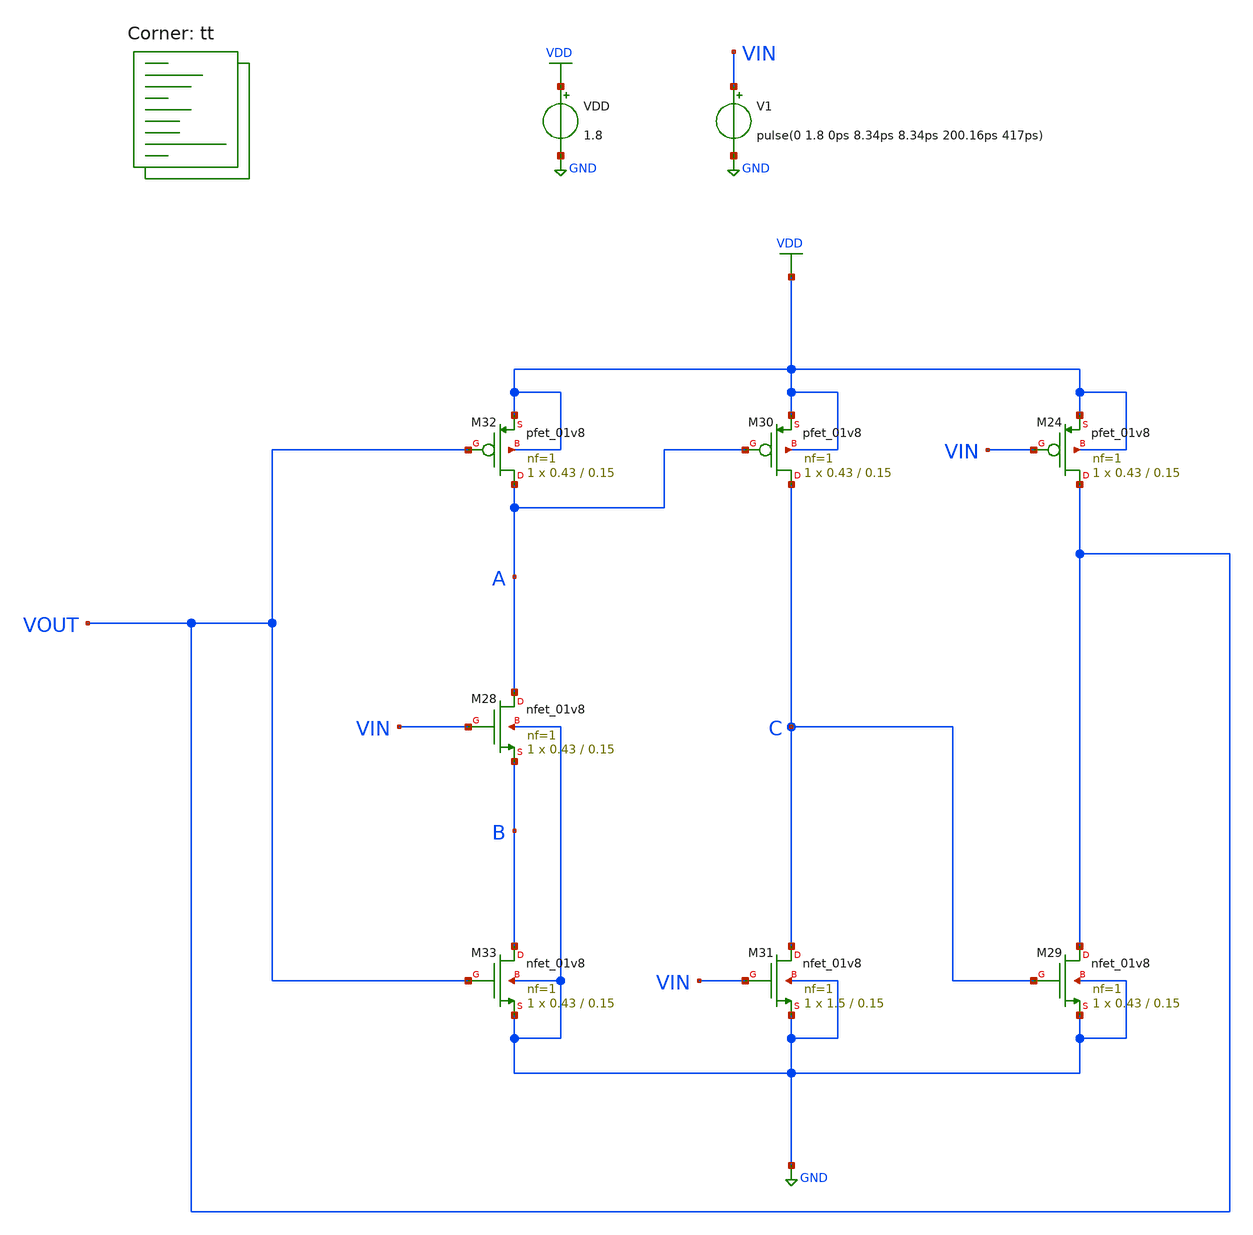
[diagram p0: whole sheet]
** sch_path: projects/pll/divider/xschem_ngspice/tb_TSPC_FF_ratioed_divide2_2.sch
**.subckt tb_TSPC_FF_ratioed_divide2_2
VDD VDD GND 1.8
V1 VIN GND pulse(0 1.8 0ps 8.34ps 8.34ps 200.16ps 417ps)
XM24 VOUT VIN VDD VDD sky130_fd_pr__pfet_01v8 L=0.15 W=0.43 nf=1 ad='int((nf+1)/2) * W/nf * 0.29' as='int((nf+2)/2) * W/nf * 0.29'
+ pd='2*int((nf+1)/2) * (W/nf + 0.29)' ps='2*int((nf+2)/2) * (W/nf + 0.29)' nrd='0.29 / W' nrs='0.29 / W'
+ sa=0 sb=0 sd=0 mult=1 m=1
XM29 VOUT C GND GND sky130_fd_pr__nfet_01v8 L=0.15 W=0.43 nf=1 ad='int((nf+1)/2) * W/nf * 0.29' as='int((nf+2)/2) * W/nf * 0.29'
+ pd='2*int((nf+1)/2) * (W/nf + 0.29)' ps='2*int((nf+2)/2) * (W/nf + 0.29)' nrd='0.29 / W' nrs='0.29 / W'
+ sa=0 sb=0 sd=0 mult=1 m=1
XM30 C A VDD VDD sky130_fd_pr__pfet_01v8 L=0.15 W=0.43 nf=1 ad='int((nf+1)/2) * W/nf * 0.29' as='int((nf+2)/2) * W/nf * 0.29'
+ pd='2*int((nf+1)/2) * (W/nf + 0.29)' ps='2*int((nf+2)/2) * (W/nf + 0.29)' nrd='0.29 / W' nrs='0.29 / W'
+ sa=0 sb=0 sd=0 mult=1 m=1
XM31 C VIN GND GND sky130_fd_pr__nfet_01v8 L=0.15 W=1.5 nf=1 ad='int((nf+1)/2) * W/nf * 0.29' as='int((nf+2)/2) * W/nf * 0.29'
+ pd='2*int((nf+1)/2) * (W/nf + 0.29)' ps='2*int((nf+2)/2) * (W/nf + 0.29)' nrd='0.29 / W' nrs='0.29 / W'
+ sa=0 sb=0 sd=0 mult=1 m=1
XM32 A VOUT VDD VDD sky130_fd_pr__pfet_01v8 L=0.15 W=0.43 nf=1 ad='int((nf+1)/2) * W/nf * 0.29' as='int((nf+2)/2) * W/nf * 0.29'
+ pd='2*int((nf+1)/2) * (W/nf + 0.29)' ps='2*int((nf+2)/2) * (W/nf + 0.29)' nrd='0.29 / W' nrs='0.29 / W'
+ sa=0 sb=0 sd=0 mult=1 m=1
XM33 B VOUT GND GND sky130_fd_pr__nfet_01v8 L=0.15 W=0.43 nf=1 ad='int((nf+1)/2) * W/nf * 0.29' as='int((nf+2)/2) * W/nf * 0.29'
+ pd='2*int((nf+1)/2) * (W/nf + 0.29)' ps='2*int((nf+2)/2) * (W/nf + 0.29)' nrd='0.29 / W' nrs='0.29 / W'
+ sa=0 sb=0 sd=0 mult=1 m=1
XM28 A VIN B GND sky130_fd_pr__nfet_01v8 L=0.15 W=0.43 nf=1 ad='int((nf+1)/2) * W/nf * 0.29' as='int((nf+2)/2) * W/nf * 0.29'
+ pd='2*int((nf+1)/2) * (W/nf + 0.29)' ps='2*int((nf+2)/2) * (W/nf + 0.29)' nrd='0.29 / W' nrs='0.29 / W'
+ sa=0 sb=0 sd=0 mult=1 m=1
**** begin user architecture code



.include /foss/pdks/sky130A/libs.ref/sky130_fd_sc_hd/spice/sky130_fd_sc_hd.spice

.option method=gear
.option wnflag=1
.option savecurrents


*.ic v(d)=0
*.ic v(q)=0
*.ic v(q1)=0

.probe p(x1)

.control

*  save v(vin) v(vout) p(x1:power)
  save all
  * save all
  * tran 0.1n 1u
  tran 0.5p 10n

  remzerovec
  write tb_TSPC_FF_ratioed_divide2_2.raw
  * set appendwrite

.endc



.lib $::SKYWATER_MODELS/sky130.lib.spice tt
**** end user architecture code
**.ends
.GLOBAL GND
.GLOBAL VDD
.end
